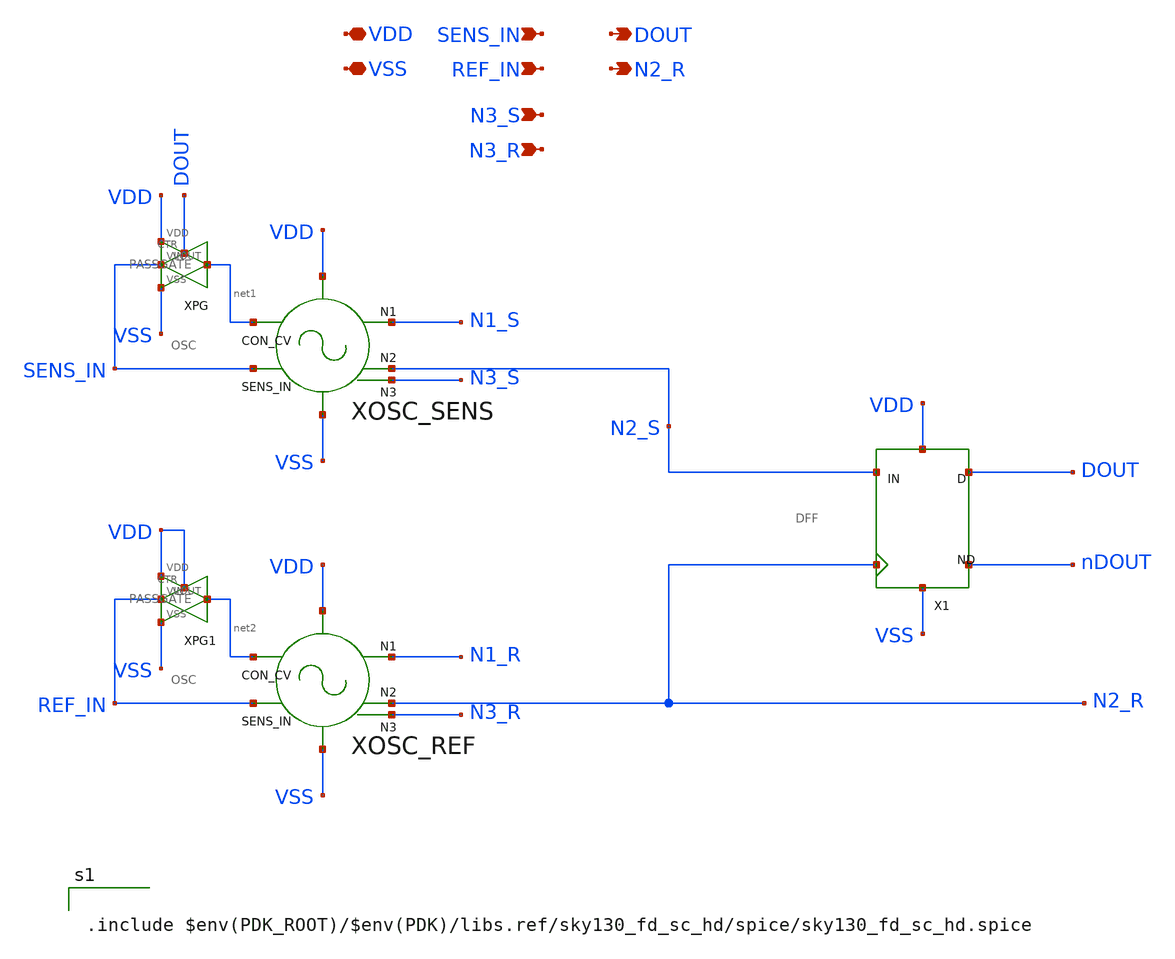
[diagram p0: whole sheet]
** sch_path: modules/INTERNAL_SDC/symbol/INTERNAL_SDC.sch
**.subckt INTERNAL_SDC VDD VSS SENS_IN REF_IN DOUT N3_S N3_R N2_R
*.iopin VDD
*.iopin VSS
*.ipin SENS_IN
*.ipin REF_IN
*.opin DOUT
*.ipin N3_S
*.ipin N3_R
*.opin N2_R
XOSC_SENS SENS_IN N1_S N2_S VDD VSS net1 N3_S OSC
XOSC_REF REF_IN N1_R N2_R VDD VSS net2 N3_R OSC
XPG SENS_IN DOUT net1 VDD VSS PASSGATE
XPG1 REF_IN VDD net2 VDD VSS PASSGATE
X1 N2_S N2_R DOUT nDOUT VDD VSS DFF
**** begin user architecture code

.include $env(PDK_ROOT)/$env(PDK)/libs.ref/sky130_fd_sc_hd/spice/sky130_fd_sc_hd.spice

**** end user architecture code
**.ends
.end
